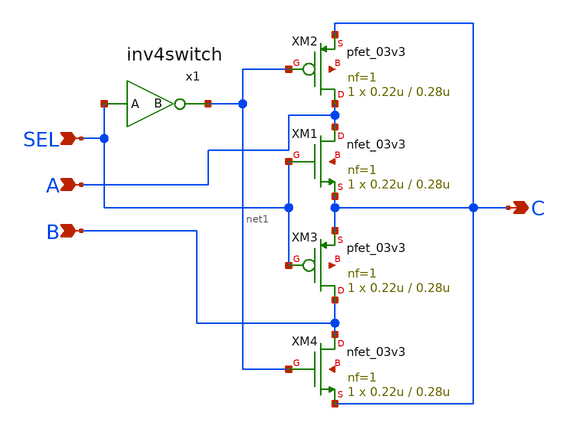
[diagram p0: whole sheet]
** sch_path: Chandra/mux_2to1.sch
**.subckt mux_2to1 A B SEL C
*.ipin A
*.ipin B
*.ipin SEL
*.opin C
XM1 A SEL C net2 nfet_03v3 L=0.28u W=0.22u nf=1 ad='int((nf+1)/2) * W/nf * 0.18u' as='int((nf+2)/2) * W/nf * 0.18u'
+ pd='2*int((nf+1)/2) * (W/nf + 0.18u)' ps='2*int((nf+2)/2) * (W/nf + 0.18u)' nrd='0.18u / W' nrs='0.18u / W'
+ sa=0 sb=0 sd=0 m=1
XM2 A net1 C net3 pfet_03v3 L=0.28u W=0.22u nf=1 ad='int((nf+1)/2) * W/nf * 0.18u' as='int((nf+2)/2) * W/nf * 0.18u'
+ pd='2*int((nf+1)/2) * (W/nf + 0.18u)' ps='2*int((nf+2)/2) * (W/nf + 0.18u)' nrd='0.18u / W' nrs='0.18u / W'
+ sa=0 sb=0 sd=0 m=1
XM3 B SEL C net4 pfet_03v3 L=0.28u W=0.22u nf=1 ad='int((nf+1)/2) * W/nf * 0.18u' as='int((nf+2)/2) * W/nf * 0.18u'
+ pd='2*int((nf+1)/2) * (W/nf + 0.18u)' ps='2*int((nf+2)/2) * (W/nf + 0.18u)' nrd='0.18u / W' nrs='0.18u / W'
+ sa=0 sb=0 sd=0 m=1
XM4 B net1 C net5 nfet_03v3 L=0.28u W=0.22u nf=1 ad='int((nf+1)/2) * W/nf * 0.18u' as='int((nf+2)/2) * W/nf * 0.18u'
+ pd='2*int((nf+1)/2) * (W/nf + 0.18u)' ps='2*int((nf+2)/2) * (W/nf + 0.18u)' nrd='0.18u / W' nrs='0.18u / W'
+ sa=0 sb=0 sd=0 m=1
x1 net1 SEL inv4switch
**.ends

* expanding   symbol:  inv4switch.sym # of pins=2
** sym_path: Chandra/inv4switch.sym
** sch_path: Chandra/inv4switch.sch
.subckt inv4switch B A
*.ipin A
*.opin B
XM1 B A 0 net1 nfet_03v3 L=0.3u W=1u nf=1 ad='int((nf+1)/2) * W/nf * 0.18u' as='int((nf+2)/2) * W/nf * 0.18u'
+ pd='2*int((nf+1)/2) * (W/nf + 0.18u)' ps='2*int((nf+2)/2) * (W/nf + 0.18u)' nrd='0.18u / W' nrs='0.18u / W'
+ sa=0 sb=0 sd=0 m=1
XM2 B A VDD net2 pfet_03v3 L=0.3u W=2u nf=1 ad='int((nf+1)/2) * W/nf * 0.18u' as='int((nf+2)/2) * W/nf * 0.18u'
+ pd='2*int((nf+1)/2) * (W/nf + 0.18u)' ps='2*int((nf+2)/2) * (W/nf + 0.18u)' nrd='0.18u / W' nrs='0.18u / W'
+ sa=0 sb=0 sd=0 m=1
.ends

.GLOBAL VDD
.end
